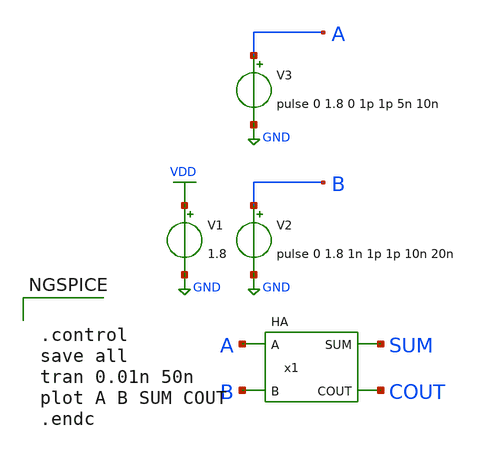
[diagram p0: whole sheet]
** sch_path: lib/xschem/test_HA.sch
**.subckt test_HA
V2 B GND pulse 0 1.8 1n 1p 1p 10n 20n
V1 VDD GND 1.8
V3 A GND pulse 0 1.8 0 1p 1p 5n 10n
x1 SUM COUT A B VDD GND HA
**** begin user architecture code

.lib $::SKYWATER_MODELS/sky130.lib.spice tt


**** end user architecture code
**.ends

* expanding   symbol:  HA.sym # of pins=4
** sym_path: lib/xschem/HA.sym
** sch_path: lib/xschem/HA.sch
.subckt HA SUM COUT A B VCCPIN VSSPIN
*.ipin A
*.ipin B
*.opin SUM
*.opin COUT
x1 SUM A B VCCPIN VSSPIN XOR2X1
x2 COUT A B VCCPIN VSSPIN AND2X1
.ends


* expanding   symbol:  XOR2X1.sym # of pins=3
** sym_path: lib/xschem/XOR2X1.sym
** sch_path: lib/xschem/XOR2X1.sch
.subckt XOR2X1 Y A B VCCPIN VSSPIN
*.ipin A
*.opin Y
*.ipin B
XM1 net6 A VSSPIN GND sky130_fd_pr__nfet_01v8 L=0.15 W=3 nf=1 ad='int((nf+1)/2) * W/nf * 0.29' as='int((nf+2)/2) * W/nf * 0.29'
+ pd='2*int((nf+1)/2) * (W/nf + 0.29)' ps='2*int((nf+2)/2) * (W/nf + 0.29)' nrd='0.29 / W' nrs='0.29 / W'
+ sa=0 sb=0 sd=0 mult=1 m=1
XM2 net6 A VCCPIN VDD sky130_fd_pr__pfet_01v8 L=0.15 W=2 nf=1 ad='int((nf+1)/2) * W/nf * 0.29' as='int((nf+2)/2) * W/nf * 0.29'
+ pd='2*int((nf+1)/2) * (W/nf + 0.29)' ps='2*int((nf+2)/2) * (W/nf + 0.29)' nrd='0.29 / W' nrs='0.29 / W'
+ sa=0 sb=0 sd=0 mult=1 m=1
XM3 net3 B VSSPIN GND sky130_fd_pr__nfet_01v8 L=0.15 W=3 nf=1 ad='int((nf+1)/2) * W/nf * 0.29' as='int((nf+2)/2) * W/nf * 0.29'
+ pd='2*int((nf+1)/2) * (W/nf + 0.29)' ps='2*int((nf+2)/2) * (W/nf + 0.29)' nrd='0.29 / W' nrs='0.29 / W'
+ sa=0 sb=0 sd=0 mult=1 m=1
XM4 net3 B VCCPIN VDD sky130_fd_pr__pfet_01v8 L=0.15 W=2 nf=1 ad='int((nf+1)/2) * W/nf * 0.29' as='int((nf+2)/2) * W/nf * 0.29'
+ pd='2*int((nf+1)/2) * (W/nf + 0.29)' ps='2*int((nf+2)/2) * (W/nf + 0.29)' nrd='0.29 / W' nrs='0.29 / W'
+ sa=0 sb=0 sd=0 mult=1 m=1
XM5 net4 net3 VCCPIN VDD sky130_fd_pr__pfet_01v8 L=0.15 W=2 nf=1 ad='int((nf+1)/2) * W/nf * 0.29' as='int((nf+2)/2) * W/nf * 0.29'
+ pd='2*int((nf+1)/2) * (W/nf + 0.29)' ps='2*int((nf+2)/2) * (W/nf + 0.29)' nrd='0.29 / W' nrs='0.29 / W'
+ sa=0 sb=0 sd=0 mult=1 m=1
XM6 Y A net4 VDD sky130_fd_pr__pfet_01v8 L=0.15 W=2 nf=1 ad='int((nf+1)/2) * W/nf * 0.29' as='int((nf+2)/2) * W/nf * 0.29'
+ pd='2*int((nf+1)/2) * (W/nf + 0.29)' ps='2*int((nf+2)/2) * (W/nf + 0.29)' nrd='0.29 / W' nrs='0.29 / W'
+ sa=0 sb=0 sd=0 mult=1 m=1
XM7 net2 B VCCPIN VDD sky130_fd_pr__pfet_01v8 L=0.15 W=2 nf=1 ad='int((nf+1)/2) * W/nf * 0.29' as='int((nf+2)/2) * W/nf * 0.29'
+ pd='2*int((nf+1)/2) * (W/nf + 0.29)' ps='2*int((nf+2)/2) * (W/nf + 0.29)' nrd='0.29 / W' nrs='0.29 / W'
+ sa=0 sb=0 sd=0 mult=1 m=1
XM8 Y net6 net2 VDD sky130_fd_pr__pfet_01v8 L=0.15 W=2 nf=1 ad='int((nf+1)/2) * W/nf * 0.29' as='int((nf+2)/2) * W/nf * 0.29'
+ pd='2*int((nf+1)/2) * (W/nf + 0.29)' ps='2*int((nf+2)/2) * (W/nf + 0.29)' nrd='0.29 / W' nrs='0.29 / W'
+ sa=0 sb=0 sd=0 mult=1 m=1
XM9 Y net6 net1 GND sky130_fd_pr__nfet_01v8 L=0.15 W=3 nf=1 ad='int((nf+1)/2) * W/nf * 0.29' as='int((nf+2)/2) * W/nf * 0.29'
+ pd='2*int((nf+1)/2) * (W/nf + 0.29)' ps='2*int((nf+2)/2) * (W/nf + 0.29)' nrd='0.29 / W' nrs='0.29 / W'
+ sa=0 sb=0 sd=0 mult=1 m=1
XM10 net1 net3 VSSPIN GND sky130_fd_pr__nfet_01v8 L=0.15 W=3 nf=1 ad='int((nf+1)/2) * W/nf * 0.29' as='int((nf+2)/2) * W/nf * 0.29'
+ pd='2*int((nf+1)/2) * (W/nf + 0.29)' ps='2*int((nf+2)/2) * (W/nf + 0.29)' nrd='0.29 / W' nrs='0.29 / W'
+ sa=0 sb=0 sd=0 mult=1 m=1
XM11 Y A net5 GND sky130_fd_pr__nfet_01v8 L=0.15 W=3 nf=1 ad='int((nf+1)/2) * W/nf * 0.29' as='int((nf+2)/2) * W/nf * 0.29'
+ pd='2*int((nf+1)/2) * (W/nf + 0.29)' ps='2*int((nf+2)/2) * (W/nf + 0.29)' nrd='0.29 / W' nrs='0.29 / W'
+ sa=0 sb=0 sd=0 mult=1 m=1
XM12 net5 B VSSPIN GND sky130_fd_pr__nfet_01v8 L=0.15 W=3 nf=1 ad='int((nf+1)/2) * W/nf * 0.29' as='int((nf+2)/2) * W/nf * 0.29'
+ pd='2*int((nf+1)/2) * (W/nf + 0.29)' ps='2*int((nf+2)/2) * (W/nf + 0.29)' nrd='0.29 / W' nrs='0.29 / W'
+ sa=0 sb=0 sd=0 mult=1 m=1
XM13 net4 net3 VCCPIN VDD sky130_fd_pr__pfet_01v8 L=0.15 W=2 nf=1 ad='int((nf+1)/2) * W/nf * 0.29' as='int((nf+2)/2) * W/nf * 0.29'
+ pd='2*int((nf+1)/2) * (W/nf + 0.29)' ps='2*int((nf+2)/2) * (W/nf + 0.29)' nrd='0.29 / W' nrs='0.29 / W'
+ sa=0 sb=0 sd=0 mult=1 m=1
XM14 Y A net4 VDD sky130_fd_pr__pfet_01v8 L=0.15 W=2 nf=1 ad='int((nf+1)/2) * W/nf * 0.29' as='int((nf+2)/2) * W/nf * 0.29'
+ pd='2*int((nf+1)/2) * (W/nf + 0.29)' ps='2*int((nf+2)/2) * (W/nf + 0.29)' nrd='0.29 / W' nrs='0.29 / W'
+ sa=0 sb=0 sd=0 mult=1 m=1
XM15 net2 B VCCPIN VDD sky130_fd_pr__pfet_01v8 L=0.15 W=2 nf=1 ad='int((nf+1)/2) * W/nf * 0.29' as='int((nf+2)/2) * W/nf * 0.29'
+ pd='2*int((nf+1)/2) * (W/nf + 0.29)' ps='2*int((nf+2)/2) * (W/nf + 0.29)' nrd='0.29 / W' nrs='0.29 / W'
+ sa=0 sb=0 sd=0 mult=1 m=1
XM16 Y net6 net2 VDD sky130_fd_pr__pfet_01v8 L=0.15 W=2 nf=1 ad='int((nf+1)/2) * W/nf * 0.29' as='int((nf+2)/2) * W/nf * 0.29'
+ pd='2*int((nf+1)/2) * (W/nf + 0.29)' ps='2*int((nf+2)/2) * (W/nf + 0.29)' nrd='0.29 / W' nrs='0.29 / W'
+ sa=0 sb=0 sd=0 mult=1 m=1
XM17 net3 B VCCPIN VDD sky130_fd_pr__pfet_01v8 L=0.15 W=2 nf=1 ad='int((nf+1)/2) * W/nf * 0.29' as='int((nf+2)/2) * W/nf * 0.29'
+ pd='2*int((nf+1)/2) * (W/nf + 0.29)' ps='2*int((nf+2)/2) * (W/nf + 0.29)' nrd='0.29 / W' nrs='0.29 / W'
+ sa=0 sb=0 sd=0 mult=1 m=1
XM18 net6 A VCCPIN VDD sky130_fd_pr__pfet_01v8 L=0.15 W=2 nf=1 ad='int((nf+1)/2) * W/nf * 0.29' as='int((nf+2)/2) * W/nf * 0.29'
+ pd='2*int((nf+1)/2) * (W/nf + 0.29)' ps='2*int((nf+2)/2) * (W/nf + 0.29)' nrd='0.29 / W' nrs='0.29 / W'
+ sa=0 sb=0 sd=0 mult=1 m=1
.ends


* expanding   symbol:  AND2X1.sym # of pins=3
** sym_path: lib/xschem/AND2X1.sym
** sch_path: lib/xschem/AND2X1.sch
.subckt AND2X1 Y A B VCCPIN VSSPIN
*.ipin A
*.ipin B
*.opin Y
x1 net1 A B NAND2X1
x2 Y net1 INVX1
.ends


* expanding   symbol:  NAND2X1.sym # of pins=3
** sym_path: lib/xschem/NAND2X1.sym
** sch_path: lib/xschem/NAND2X1.sch
.subckt NAND2X1 Y A B
*.ipin A
*.opin Y
*.ipin B
XM1 Y A VDD VDD sky130_fd_pr__pfet_01v8 L=0.15 W=2 nf=1 ad='int((nf+1)/2) * W/nf * 0.29' as='int((nf+2)/2) * W/nf * 0.29'
+ pd='2*int((nf+1)/2) * (W/nf + 0.29)' ps='2*int((nf+2)/2) * (W/nf + 0.29)' nrd='0.29 / W' nrs='0.29 / W'
+ sa=0 sb=0 sd=0 mult=1 m=1
XM5 Y A net1 VSS sky130_fd_pr__nfet_01v8 L=0.15 W=3 nf=1 ad='int((nf+1)/2) * W/nf * 0.29' as='int((nf+2)/2) * W/nf * 0.29'
+ pd='2*int((nf+1)/2) * (W/nf + 0.29)' ps='2*int((nf+2)/2) * (W/nf + 0.29)' nrd='0.29 / W' nrs='0.29 / W'
+ sa=0 sb=0 sd=0 mult=1 m=1
XM2 Y A VDD VDD sky130_fd_pr__pfet_01v8 L=0.15 W=2 nf=1 ad='int((nf+1)/2) * W/nf * 0.29' as='int((nf+2)/2) * W/nf * 0.29'
+ pd='2*int((nf+1)/2) * (W/nf + 0.29)' ps='2*int((nf+2)/2) * (W/nf + 0.29)' nrd='0.29 / W' nrs='0.29 / W'
+ sa=0 sb=0 sd=0 mult=1 m=1
XM3 Y B VDD VDD sky130_fd_pr__pfet_01v8 L=0.15 W=2 nf=1 ad='int((nf+1)/2) * W/nf * 0.29' as='int((nf+2)/2) * W/nf * 0.29'
+ pd='2*int((nf+1)/2) * (W/nf + 0.29)' ps='2*int((nf+2)/2) * (W/nf + 0.29)' nrd='0.29 / W' nrs='0.29 / W'
+ sa=0 sb=0 sd=0 mult=1 m=1
XM4 Y B VDD VDD sky130_fd_pr__pfet_01v8 L=0.15 W=2 nf=1 ad='int((nf+1)/2) * W/nf * 0.29' as='int((nf+2)/2) * W/nf * 0.29'
+ pd='2*int((nf+1)/2) * (W/nf + 0.29)' ps='2*int((nf+2)/2) * (W/nf + 0.29)' nrd='0.29 / W' nrs='0.29 / W'
+ sa=0 sb=0 sd=0 mult=1 m=1
XM6 net1 B VSS VSS sky130_fd_pr__nfet_01v8 L=0.15 W=3 nf=1 ad='int((nf+1)/2) * W/nf * 0.29' as='int((nf+2)/2) * W/nf * 0.29'
+ pd='2*int((nf+1)/2) * (W/nf + 0.29)' ps='2*int((nf+2)/2) * (W/nf + 0.29)' nrd='0.29 / W' nrs='0.29 / W'
+ sa=0 sb=0 sd=0 mult=1 m=1
.ends

.GLOBAL VDD
.GLOBAL GND
**** begin user architecture code


.control
save all
tran 0.01n 50n
plot A B SUM COUT
.endc


**** end user architecture code
.end
